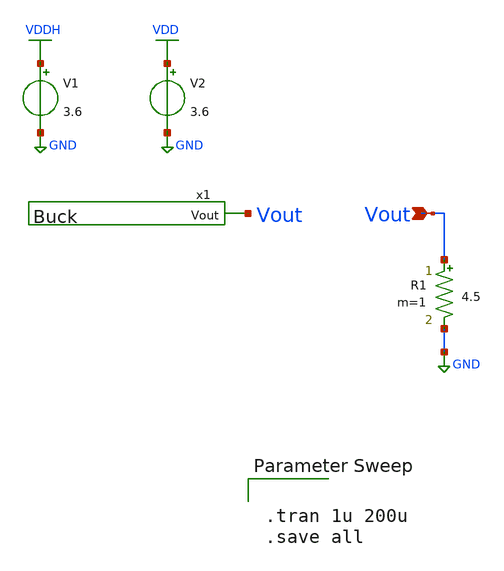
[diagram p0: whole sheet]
** sch_path: Ene_Thompson/test_Buck.sch
**.subckt test_Buck Vout
*.ipin Vout
x1 Vout Buck
V1 VDDH GND 3.6
R1 Vout GND 4.5 m=1
V2 VDD GND 3.6
**** begin user architecture code

.lib $::SKYWATER_MODELS/sky130.lib.spice tt


.tran 1u 200u
.save all



.subckt sky130_fd_sc_hd__nand2_1 A B VGND VNB VPB VPWR Y
X0 Y A VPWR VPB sky130_fd_pr__pfet_g5v0d10v5 w=1 l=0.5
X1 VPWR B Y VPB sky130_fd_pr__pfet_g5v0d10v5 w=1 l=0.5
X2 VGND B a_113_47# VNB sky130_fd_pr__nfet_g5v0d10v5 w=1 l=0.5
X3 a_113_47# A Y VNB sky130_fd_pr__nfet_g5v0d10v5 w=1 l=0.5
.ends

.subckt sky130_fd_sc_hd__inv_1 A VGND VNB VPB VPWR Y
X0 VGND A Y VNB sky130_fd_pr__nfet_g5v0d10v5 w=1 l=0.5
X1 VPWR A Y VPB sky130_fd_pr__pfet_g5v0d10v5 w=1 l=0.5
.ends

**** end user architecture code
**.ends

* expanding   symbol:  Buck.sym # of pins=1
** sym_path: Ene_Thompson/Buck.sym
** sch_path: Ene_Thompson/Buck.sch
.subckt Buck Vout
*.opin Vout
XM1 vl pswitch VDD VDD sky130_fd_pr__pfet_g5v0d10v5 L=0.5 W=20 nf=1 ad='int((nf+1)/2) * W/nf * 0.29'
+ as='int((nf+2)/2) * W/nf * 0.29' pd='2*int((nf+1)/2) * (W/nf + 0.29)' ps='2*int((nf+2)/2) * (W/nf + 0.29)'
+ nrd='0.29 / W' nrs='0.29 / W' sa=0 sb=0 sd=0 mult=1000 m=1000
XM2 vl nswitch GND GND sky130_fd_pr__nfet_g5v0d10v5 L=0.5 W=20 nf=1 ad='int((nf+1)/2) * W/nf * 0.29'
+ as='int((nf+2)/2) * W/nf * 0.29' pd='2*int((nf+1)/2) * (W/nf + 0.29)' ps='2*int((nf+2)/2) * (W/nf + 0.29)'
+ nrd='0.29 / W' nrs='0.29 / W' sa=0 sb=0 sd=0 mult=1000 m=1000
L1 net2 Vout 4.7u m=1
C1 Vout net1 1u m=1
V1 pswitch GND PULSE(0 5 0 0.01u 0.01u 0.5u 1u)
R1 vl net2 1.5m m=1
R2 GND net1 10m m=1
V2 nswitch GND PULSE(0 5 50n 0.01u 0.01u 0.55u 1u)
.ends

.GLOBAL VDDH
.GLOBAL GND
.GLOBAL VDD
.end
